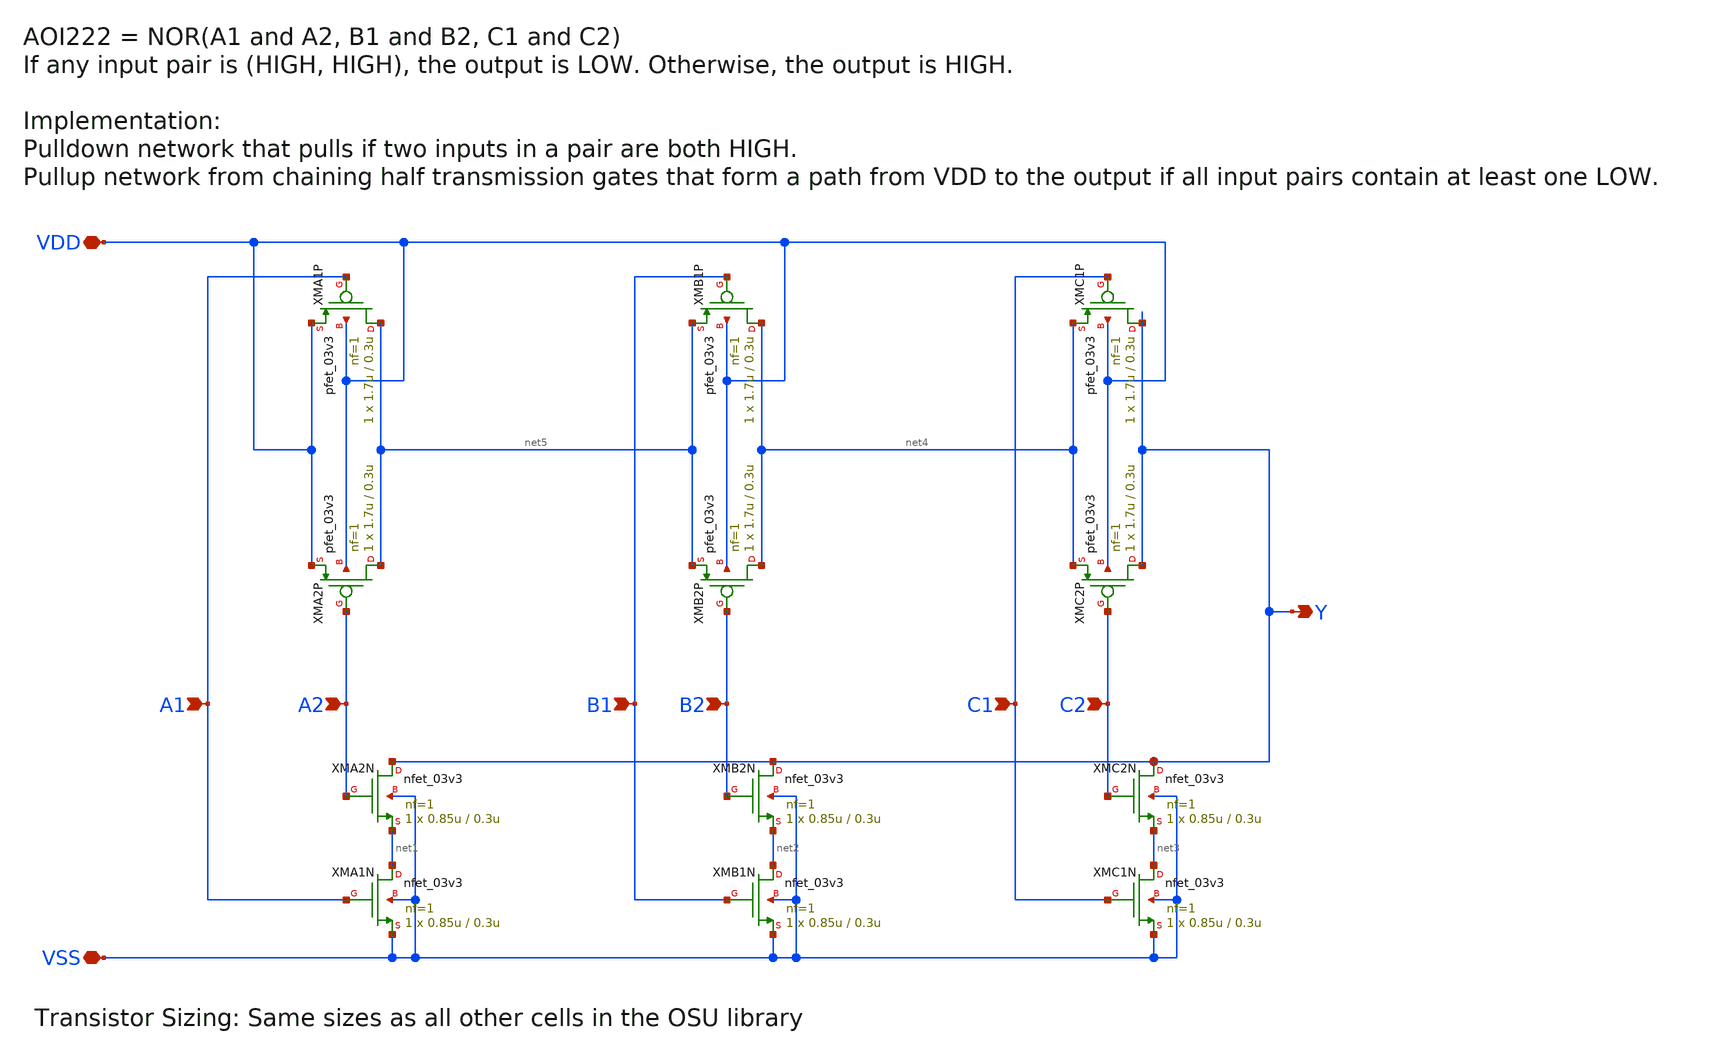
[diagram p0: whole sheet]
** sch_path: gf180mcu_osu_sc_gp12t3v3/xschem/gf180mcu_osu_sc_gp12t3v3__aoi222_1.sch
**.subckt gf180mcu_osu_sc_gp12t3v3__aoi222_1 A1 Y B1 C1 VDD B2 C2 A2 VSS
*.ipin A1
*.opin Y
*.ipin B1
*.ipin C1
*.iopin VDD
*.ipin B2
*.ipin C2
*.ipin A2
*.iopin VSS
XMA2N Y A2 net1 VSS nfet_03v3 L=0.3u W=0.85u nf=1 ad='int((nf+1)/2) * W/nf * 0.18u' as='int((nf+2)/2) * W/nf * 0.18u'
+ pd='2*int((nf+1)/2) * (W/nf + 0.18u)' ps='2*int((nf+2)/2) * (W/nf + 0.18u)' nrd='0.18u / W' nrs='0.18u / W'
+ sa=0 sb=0 sd=0 m=1
XMA1N net1 A1 VSS VSS nfet_03v3 L=0.3u W=0.85u nf=1 ad='int((nf+1)/2) * W/nf * 0.18u' as='int((nf+2)/2) * W/nf * 0.18u'
+ pd='2*int((nf+1)/2) * (W/nf + 0.18u)' ps='2*int((nf+2)/2) * (W/nf + 0.18u)' nrd='0.18u / W' nrs='0.18u / W'
+ sa=0 sb=0 sd=0 m=1
XMA1P net5 A1 VDD VDD pfet_03v3 L=0.3u W=1.7u nf=1 ad='int((nf+1)/2) * W/nf * 0.18u' as='int((nf+2)/2) * W/nf * 0.18u'
+ pd='2*int((nf+1)/2) * (W/nf + 0.18u)' ps='2*int((nf+2)/2) * (W/nf + 0.18u)' nrd='0.18u / W' nrs='0.18u / W'
+ sa=0 sb=0 sd=0 m=1
XMA2P net5 A2 VDD VDD pfet_03v3 L=0.3u W=1.7u nf=1 ad='int((nf+1)/2) * W/nf * 0.18u' as='int((nf+2)/2) * W/nf * 0.18u'
+ pd='2*int((nf+1)/2) * (W/nf + 0.18u)' ps='2*int((nf+2)/2) * (W/nf + 0.18u)' nrd='0.18u / W' nrs='0.18u / W'
+ sa=0 sb=0 sd=0 m=1
XMB2N Y B2 net2 VSS nfet_03v3 L=0.3u W=0.85u nf=1 ad='int((nf+1)/2) * W/nf * 0.18u' as='int((nf+2)/2) * W/nf * 0.18u'
+ pd='2*int((nf+1)/2) * (W/nf + 0.18u)' ps='2*int((nf+2)/2) * (W/nf + 0.18u)' nrd='0.18u / W' nrs='0.18u / W'
+ sa=0 sb=0 sd=0 m=1
XMB1N net2 B1 VSS VSS nfet_03v3 L=0.3u W=0.85u nf=1 ad='int((nf+1)/2) * W/nf * 0.18u' as='int((nf+2)/2) * W/nf * 0.18u'
+ pd='2*int((nf+1)/2) * (W/nf + 0.18u)' ps='2*int((nf+2)/2) * (W/nf + 0.18u)' nrd='0.18u / W' nrs='0.18u / W'
+ sa=0 sb=0 sd=0 m=1
XMB1P net4 B1 net5 VDD pfet_03v3 L=0.3u W=1.7u nf=1 ad='int((nf+1)/2) * W/nf * 0.18u' as='int((nf+2)/2) * W/nf * 0.18u'
+ pd='2*int((nf+1)/2) * (W/nf + 0.18u)' ps='2*int((nf+2)/2) * (W/nf + 0.18u)' nrd='0.18u / W' nrs='0.18u / W'
+ sa=0 sb=0 sd=0 m=1
XMB2P net4 B2 net5 VDD pfet_03v3 L=0.3u W=1.7u nf=1 ad='int((nf+1)/2) * W/nf * 0.18u' as='int((nf+2)/2) * W/nf * 0.18u'
+ pd='2*int((nf+1)/2) * (W/nf + 0.18u)' ps='2*int((nf+2)/2) * (W/nf + 0.18u)' nrd='0.18u / W' nrs='0.18u / W'
+ sa=0 sb=0 sd=0 m=1
XMC2N Y C2 net3 VSS nfet_03v3 L=0.3u W=0.85u nf=1 ad='int((nf+1)/2) * W/nf * 0.18u' as='int((nf+2)/2) * W/nf * 0.18u'
+ pd='2*int((nf+1)/2) * (W/nf + 0.18u)' ps='2*int((nf+2)/2) * (W/nf + 0.18u)' nrd='0.18u / W' nrs='0.18u / W'
+ sa=0 sb=0 sd=0 m=1
XMC1N net3 C1 VSS VSS nfet_03v3 L=0.3u W=0.85u nf=1 ad='int((nf+1)/2) * W/nf * 0.18u' as='int((nf+2)/2) * W/nf * 0.18u'
+ pd='2*int((nf+1)/2) * (W/nf + 0.18u)' ps='2*int((nf+2)/2) * (W/nf + 0.18u)' nrd='0.18u / W' nrs='0.18u / W'
+ sa=0 sb=0 sd=0 m=1
XMC1P Y C1 net4 VDD pfet_03v3 L=0.3u W=1.7u nf=1 ad='int((nf+1)/2) * W/nf * 0.18u' as='int((nf+2)/2) * W/nf * 0.18u'
+ pd='2*int((nf+1)/2) * (W/nf + 0.18u)' ps='2*int((nf+2)/2) * (W/nf + 0.18u)' nrd='0.18u / W' nrs='0.18u / W'
+ sa=0 sb=0 sd=0 m=1
XMC2P Y C2 net4 VDD pfet_03v3 L=0.3u W=1.7u nf=1 ad='int((nf+1)/2) * W/nf * 0.18u' as='int((nf+2)/2) * W/nf * 0.18u'
+ pd='2*int((nf+1)/2) * (W/nf + 0.18u)' ps='2*int((nf+2)/2) * (W/nf + 0.18u)' nrd='0.18u / W' nrs='0.18u / W'
+ sa=0 sb=0 sd=0 m=1
**.ends
.end
